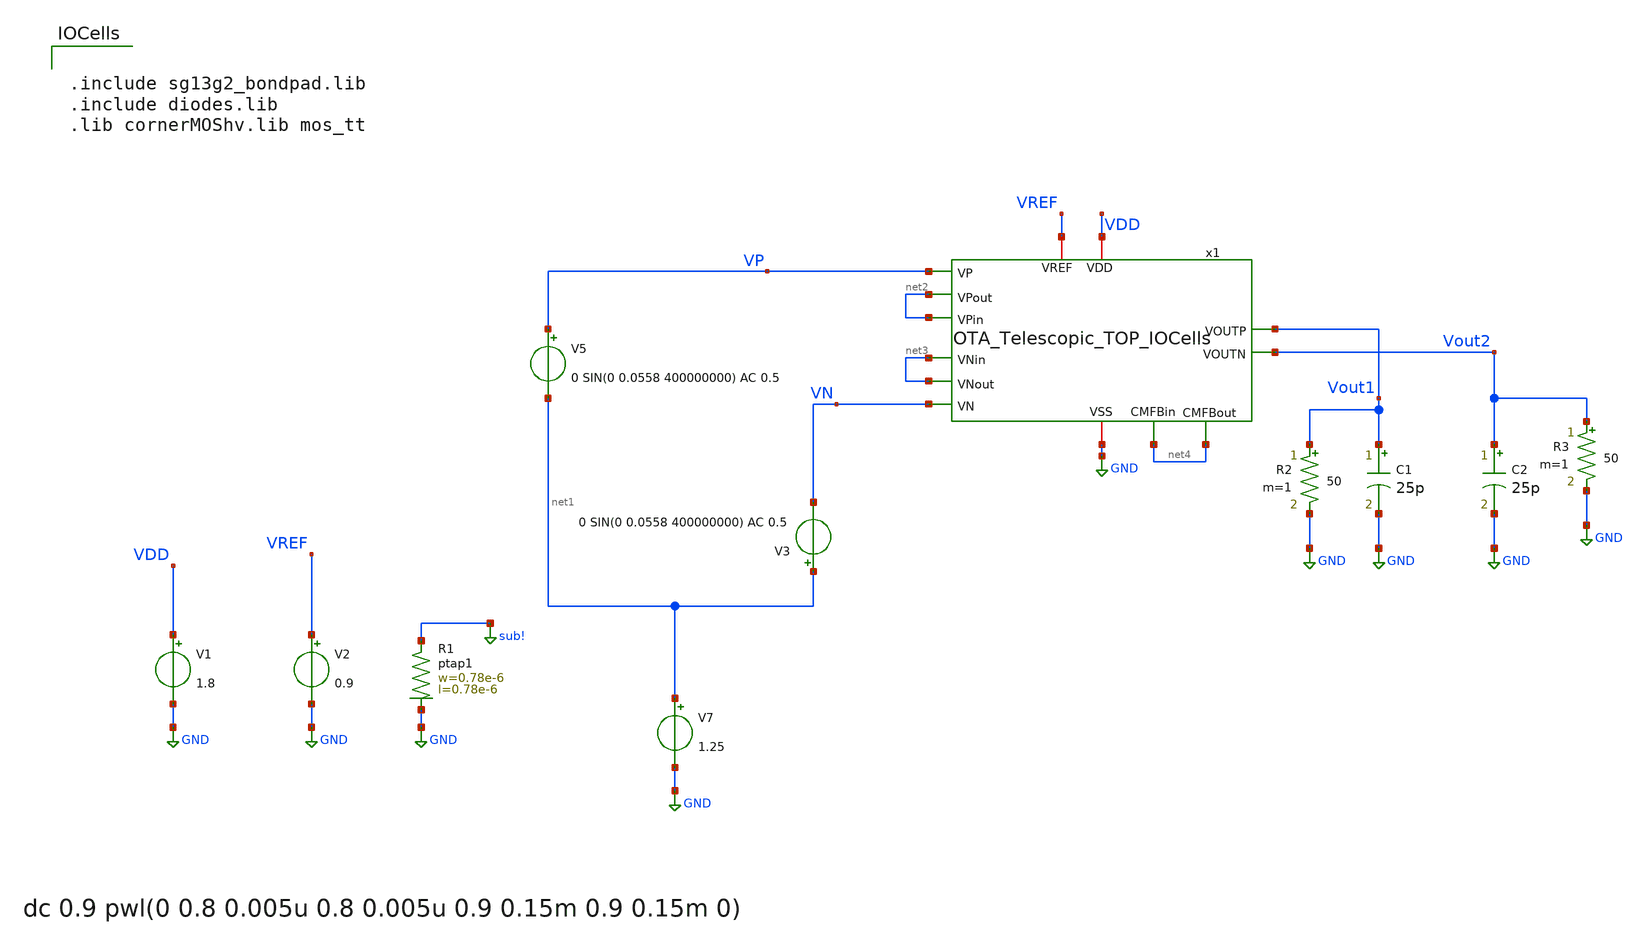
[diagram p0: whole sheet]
** sch_path: OTA_Telescopic/Testbenchs/OTA_Telescopic_TOP_TB_CL_io.sch
**.subckt OTA_Telescopic_TOP_TB_CL_io
V7 net1 GND 1.25
V5 VP net1 0 SIN(0 0.0558 400000000) AC 0.5
V1 VDD GND 1.8
V2 VREF GND 0.9
C1 Vout1 GND 25p m=1
C2 Vout2 GND 25p m=1
V3 net1 VN 0 SIN(0 0.0558 400000000) AC 0.5
x1 VDD GND net2 VP net2 Vout2 Vout1 net3 net3 VN VREF net4 net4 OTA_Telescopic_TOP_IOCells
XR1 sub! GND ptap1 R=262.8 w=0.78e-6 l=0.78e-6
R2 Vout1 GND 50 m=1
R3 Vout2 GND 50 m=1
**** begin user architecture code

** opencircuitdesign pdks install
.lib cornerMOSlv.lib mos_tt
.lib cornerRES.lib res_typ
.lib cornerCAP.lib cap_typ
.temp 65



.control
save all
 set color0 = white

* AC simulation
ac dec 1000 1 1T
let Av = db(v(Vout1)-v(Vout2))
meas ac Ao FIND Av WHEN frequency=10
let ABW = Ao-3
meas ac BW WHEN Av=ABW
meas ac UGBW WHEN Av=0
let phase_vec = 180/pi*cph(v(Vout1)-v(Vout2))

* Phase margin (PM)
meas ac phase FIND phase_vec WHEN frequency=UGBW
let PM = phase+180
print PM

* Gain margin (GM)
meas ac freq180 FIND frequency WHEN phase_vec=-180
meas ac gain FIND Av WHEN frequency=freq180
let GM = 0-gain

print GM
plot Av
plot phase_vec

write AC_OL.raw
wrdata AvCL_ Av

*DC simulation

op
let vout_dc = v(Vout1)
print vout_dc
write OTA_Telescopic_TOP_TB_CL.raw

.endc




.include sg13g2_bondpad.lib
.include diodes.lib
.lib cornerMOShv.lib mos_tt


**** end user architecture code
**.ends
.GLOBAL GND
.GLOBAL sub!
.end
